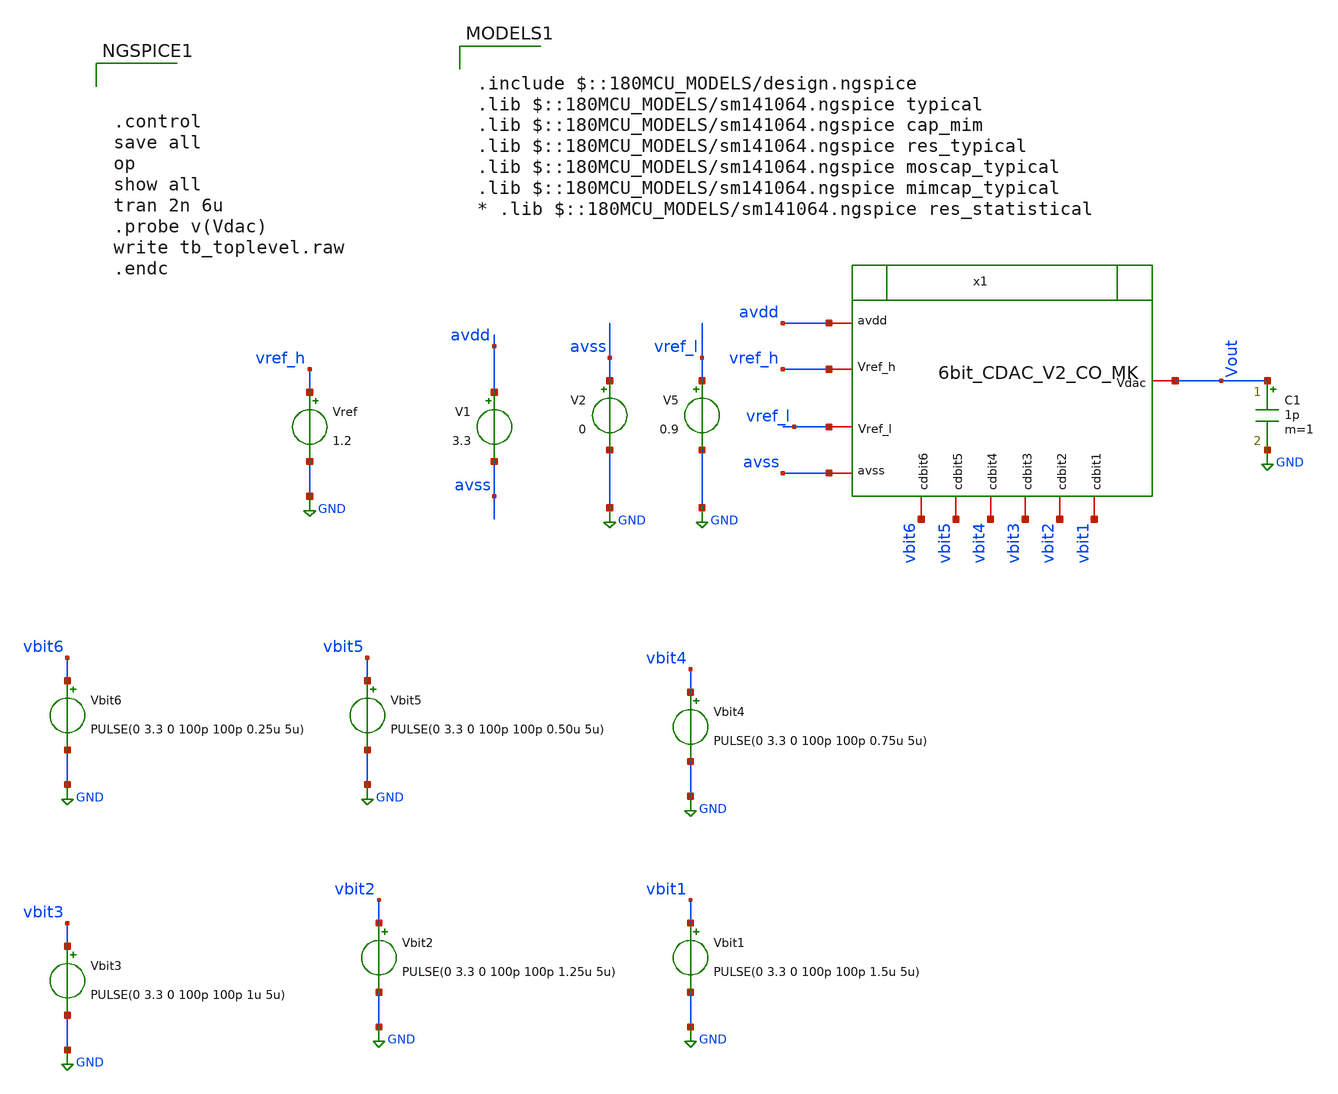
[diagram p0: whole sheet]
** sch_path: designs/full_ADC/tb_toplevel.sch
**.subckt tb_toplevel
V1 avdd avss 3.3
V2 avss GND 0
Vbit1 vbit1 GND PULSE(0 3.3 0 100p 100p 1.5u 5u)
Vbit2 vbit2 GND PULSE(0 3.3 0 100p 100p 1.25u 5u)
Vbit3 vbit3 GND PULSE(0 3.3 0 100p 100p 1u 5u)
Vbit4 vbit4 GND PULSE(0 3.3 0 100p 100p 0.75u 5u)
Vbit5 vbit5 GND PULSE(0 3.3 0 100p 100p 0.50u 5u)
Vbit6 vbit6 GND PULSE(0 3.3 0 100p 100p 0.25u 5u)
Vref vref_h GND 1.2
C1 Vout GND 1p m=1
x1 vref_l Vout avdd avss vref_h vbit6 vbit5 vbit3 vbit1 vbit2 vbit4 6bit_CDAC_V2_CO_MK
V5 vref_l GND 0.9
**** begin user architecture code



.control
save all
op
show all
tran 2n 6u
.probe v(Vdac)
write tb_toplevel.raw
.endc



.include $::180MCU_MODELS/design.ngspice
.lib $::180MCU_MODELS/sm141064.ngspice typical
.lib $::180MCU_MODELS/sm141064.ngspice cap_mim
.lib $::180MCU_MODELS/sm141064.ngspice res_typical
.lib $::180MCU_MODELS/sm141064.ngspice moscap_typical
.lib $::180MCU_MODELS/sm141064.ngspice mimcap_typical
* .lib $::180MCU_MODELS/sm141064.ngspice res_statistical

**** end user architecture code
**.ends

* expanding   symbol:  libs/WK_Kadam/6bit_CDAC_V2_CO_MK.sym # of pins=11
** sym_path: designs/libs/WK_Kadam/6bit_CDAC_V2_CO_MK.sym
** sch_path: designs/libs/WK_Kadam/6bit_CDAC_V2_CO_MK.sch
.subckt 6bit_CDAC_V2_CO_MK Vref_l Vdac avdd avss Vref_h cdbit6 cdbit5 cdbit3 cdbit1 cdbit2 cdbit4
*.iopin Vref_h
*.iopin Vdac
*.iopin avdd
*.iopin avss
*.iopin cdbit6
*.iopin cdbit5
*.iopin cdbit4
*.iopin cdbit3
*.iopin cdbit2
*.iopin cdbit1
*.iopin Vref_l
XC3 Vdac net2 cap_mim_2f0_m3m4_noshield c_width=10e-6 c_length=10e-6 m=4
XC4 Vdac net3 cap_mim_2f0_m3m4_noshield c_width=10e-6 c_length=10e-6 m=8
XC5 Vdac net4 cap_mim_2f0_m3m4_noshield c_width=10e-6 c_length=10e-6 m=16
XC6 Vdac net5 cap_mim_2f0_m3m4_noshield c_width=10e-6 c_length=10e-6 m=32
XC7 Vdac net6 cap_mim_2f0_m3m4_noshield c_width=10e-6 c_length=10e-6 m=64
XC1 Vdac avss cap_mim_2f0_m3m4_noshield c_width=10e-6 c_length=10e-6 m=2
XC2 Vdac net1 cap_mim_2f0_m3m4_noshield c_width=10e-6 c_length=10e-6 m=2
x1 net6 cdbit6 avss avdd Vref_h Vref_l c_dac2_switch
x2 net5 cdbit5 avss avdd Vref_h Vref_l c_dac2_switch
x3 net4 cdbit4 avss avdd Vref_h Vref_l c_dac2_switch
x4 net3 cdbit3 avss avdd Vref_h Vref_l c_dac2_switch
x5 net2 cdbit2 avss avdd Vref_h Vref_l c_dac2_switch
x6 net1 cdbit1 avss avdd Vref_h Vref_l c_dac2_switch
.ends


* expanding   symbol:  libs/WK_Kadam/c_dac2_switch.sym # of pins=6
** sym_path: designs/libs/WK_Kadam/c_dac2_switch.sym
** sch_path: designs/libs/WK_Kadam/c_dac2_switch.sch
.subckt c_dac2_switch sw_vout sw_bit avss avdd sw_Vref vreflow
*.iopin avdd
*.iopin avss
*.iopin sw_bit
*.iopin sw_vout
*.iopin sw_Vref
*.iopin vreflow
XM1 sw_vout sw_bit sw_Vref avss nfet_03v3 L=0.28u W=2u nf=1 ad='int((nf+1)/2) * W/nf * 0.18u' as='int((nf+2)/2) * W/nf * 0.18u'
+ pd='2*int((nf+1)/2) * (W/nf + 0.18u)' ps='2*int((nf+2)/2) * (W/nf + 0.18u)' nrd='0.18u / W' nrs='0.18u / W'
+ sa=0 sb=0 sd=0 m=1
XM3 sw_vout net1 vreflow avss nfet_03v3 L=0.28u W=2u nf=1 ad='int((nf+1)/2) * W/nf * 0.18u' as='int((nf+2)/2) * W/nf * 0.18u'
+ pd='2*int((nf+1)/2) * (W/nf + 0.18u)' ps='2*int((nf+2)/2) * (W/nf + 0.18u)' nrd='0.18u / W' nrs='0.18u / W'
+ sa=0 sb=0 sd=0 m=1
XM4 vreflow sw_bit sw_vout avdd pfet_03v3 L=0.28u W=2u nf=1 ad='int((nf+1)/2) * W/nf * 0.18u' as='int((nf+2)/2) * W/nf * 0.18u'
+ pd='2*int((nf+1)/2) * (W/nf + 0.18u)' ps='2*int((nf+2)/2) * (W/nf + 0.18u)' nrd='0.18u / W' nrs='0.18u / W'
+ sa=0 sb=0 sd=0 m=1
XM2 sw_Vref net1 sw_vout avdd pfet_03v3 L=0.28u W=2u nf=1 ad='int((nf+1)/2) * W/nf * 0.18u' as='int((nf+2)/2) * W/nf * 0.18u'
+ pd='2*int((nf+1)/2) * (W/nf + 0.18u)' ps='2*int((nf+2)/2) * (W/nf + 0.18u)' nrd='0.18u / W' nrs='0.18u / W'
+ sa=0 sb=0 sd=0 m=1
x1v avdd sw_bit net1 avss inv_test
.ends


* expanding   symbol:  libs/WK_Kadam/inv_test.sym # of pins=4
** sym_path: libs/WK_Kadam/inv_test.sym
** sch_path: libs/WK_Kadam/inv_test.sch
.subckt inv_test avdd in out avss
*.iopin avdd
*.iopin avss
*.iopin in
*.iopin out
XM3 out in avss avss nfet_03v3 L=0.28u W=1u nf=1 ad='int((nf+1)/2) * W/nf * 0.18u' as='int((nf+2)/2) * W/nf * 0.18u'
+ pd='2*int((nf+1)/2) * (W/nf + 0.18u)' ps='2*int((nf+2)/2) * (W/nf + 0.18u)' nrd='0.18u / W' nrs='0.18u / W'
+ sa=0 sb=0 sd=0 m=1
XM4 out in avdd avdd pfet_03v3 L=0.28u W=2.5u nf=1 ad='int((nf+1)/2) * W/nf * 0.18u' as='int((nf+2)/2) * W/nf * 0.18u'
+ pd='2*int((nf+1)/2) * (W/nf + 0.18u)' ps='2*int((nf+2)/2) * (W/nf + 0.18u)' nrd='0.18u / W' nrs='0.18u / W'
+ sa=0 sb=0 sd=0 m=1
.ends

.GLOBAL GND
.end
